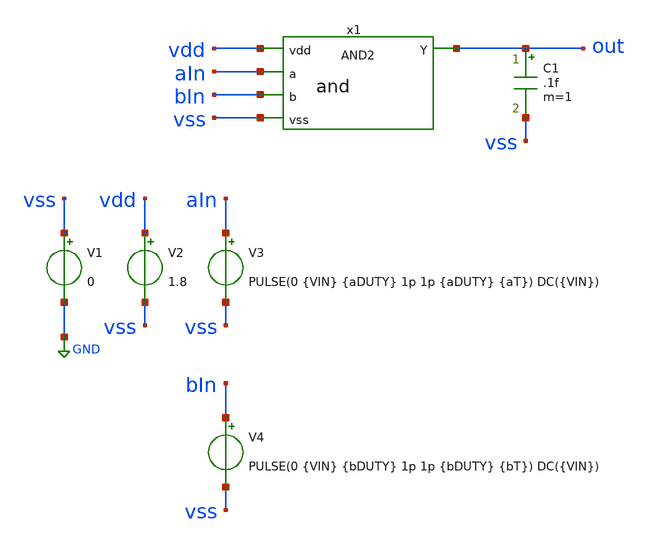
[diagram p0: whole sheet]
** sch_path: eamta2021/sch/and/tbAnd.sch
**.subckt tbAnd
V1 vss GND 0
V2 vdd vss 1.8
V3 aIn vss PULSE(0 {VIN} {aDUTY} 1p 1p {aDUTY} {aT}) DC({VIN})
C1 out vss .1f m=1
V4 bIn vss PULSE(0 {VIN} {bDUTY} 1p 1p {bDUTY} {bT}) DC({VIN})
x1 vdd out aIn bIn vss and
**** begin user architecture code



* parametros
.param VIN=1.8 aT=100n aDUTY=50n bT=200n bDUTY=100n WN=.450 WP=.90
.options TEMP=27.0

* include corners
.lib /home/eamta/skywater/skywater-pdk/libraries/sky130_fd_pr_ngspice/latest/models/corners/sky130.lib TT

* saves
.save all
**PFETs  @M.x1.xm1.msky130_fd_pr__pfet_01v8[id]  @M.x1.xm1.msky130_fd_pr__pfet_01v8[vds]
*+  @M.x1.xm1.msky130_fd_pr__pfet_01v8[vgs]  @M.x1.xm1.msky130_fd_pr__pfet_01v8[vth]  @M.x1.xm2.msky130_fd_pr__pfet_01v8[id]
*+  @M.x1.xm2.msky130_fd_pr__pfet_01v8[vds]  @M.x1.xm2.msky130_fd_pr__pfet_01v8[vgs]  @M.x1.xm2.msky130_fd_pr__pfet_01v8[vth]
*+  @M.x1.xm5.msky130_fd_pr__pfet_01v8[id]  @M.x1.xm5.msky130_fd_pr__pfet_01v8[vds]  @M.x1.xm5.msky130_fd_pr__pfet_01v8[vgs]
*+  @M.x1.xm5.msky130_fd_pr__pfet_01v8[vth]
**NFETs  @M.x1.xm3.msky130_fd_pr__nfet_01v8[id]  @M.x1.xm3.msky130_fd_pr__nfet_01v8[vds]
*+  @M.x1.xm3.msky130_fd_pr__nfet_01v8[vgs]  @M.x1.xm3.msky130_fd_pr__nfet_01v8[vth]  @M.x1.xm4.msky130_fd_pr__nfet_01v8[id]
*+  @M.x1.xm4.msky130_fd_pr__nfet_01v8[vds]  @M.x1.xm4.msky130_fd_pr__nfet_01v8[vgs]  @M.x1.xm4.msky130_fd_pr__nfet_01v8[vth]
*+  @M.x1.xm6.msky130_fd_pr__nfet_01v8[id]  @M.x1.xm6.msky130_fd_pr__nfet_01v8[vds]  @M.x1.xm6.msky130_fd_pr__nfet_01v8[vgs]
*+  @M.x1.xm6.msky130_fd_pr__nfet_01v8[vth]

* SIM
.control
	******************************************************
	*let At=.005ns

	tran 0.005ns 500ns

	setplot tran1
	**comportamiento iiiiiiiiiiiiiiiiiiiiiiiii
	plot v(aIn) v(bIn)+2 v(out)+4
	**rise/fall
	plot v(out) v(aIn) .18 1.62 xlimit 149.95ns 150.15ns
	plot v(out) v(aIn) .18 1.62 xlimit 199.95ns 200.05ns
	**sos inimputable iiiiiiiiiiiiiiiiiii
	*plot tran1.@M.x1.xm1.msky130_fd_pr__nfet_01v8[vds]
	*plot tran1.@M.x1.xm1.msky130_fd_pr__nfet_01v8[id] tran1.@M.x1.xm2.msky130_fd_pr__pfet_01v8[id]

	*set filetype=ascii iiiiiiiiiiiiiiiiiii
	*write simInvTran.raw
	*reset
	******************************************************
	*alterparam bDUTY=100n
	*dc V3 0 1.8 0.01
	*alterparam aDUTY=100n
	*dc V4 0 1.8 0.01
	*dc V3 0 1.8 0.01 V4 0 1.8 0.01

	*setplot dc1iiiiiiiiiiiiii
	*plot dc1.out vs dc1.aIn dc2.out vs dc2.bIn dc3.out vs dc3.aIn
	*plot @M.x1.xm1.msky130_fd_pr__nfet_01v8[id]
	*plot @M.x1.xm1.msky130_fd_pr__nfet_01v8[vd]

	*set filetype=ascii
	*write simInvDc.raw
	*reset
	******************************************************
	op

	set filetype=ascii
	write simInvOp.raw

***********************************************************
	*analisis cuasi parametrico
	*let actParam=1ps
	*let topParam=100ps
	*let detlaParam=10ps

	*foreach x 1ps 10ps 20ps 30ps 40ps 50ps
	*	alterparam THL=$x
	*	tran .01ns .1us
	*	let actParam=actParam+deltaParam
	*	print $x
	*end

	*plot tran1.out tran2.out tran3.out tran4.out tran5.out tran6.out tran7.out tran8.out tran9.out

	print all
.endc

.end


**** end user architecture code
**.ends

* expanding   symbol:  and/and.sym # of pins=5
** sym_path: eamta2021/sch/and/and.sym
** sch_path: eamta2021/sch/and/and.sch
.subckt and vdd Y a b vss
*.ipin vdd
*.ipin vss
*.ipin a
*.ipin b
*.opin Y
XM1 net1 b vdd vdd sky130_fd_pr__pfet_01v8 L=0.15 W={WP} nf=1 ad='int((nf+1)/2) * W/nf * 0.29' as='int((nf+2)/2) * W/nf * 0.29'
+ pd='2*int((nf+1)/2) * (W/nf + 0.29)' ps='2*int((nf+2)/2) * (W/nf + 0.29)' nrd='0.29 / W' nrs='0.29 / W'
+ sa=0 sb=0 sd=0 mult=1 m=1
XM2 net1 a vdd vdd sky130_fd_pr__pfet_01v8 L=0.15 W={WP} nf=1 ad='int((nf+1)/2) * W/nf * 0.29' as='int((nf+2)/2) * W/nf * 0.29'
+ pd='2*int((nf+1)/2) * (W/nf + 0.29)' ps='2*int((nf+2)/2) * (W/nf + 0.29)' nrd='0.29 / W' nrs='0.29 / W'
+ sa=0 sb=0 sd=0 mult=1 m=1
XM3 net1 a net2 vss sky130_fd_pr__nfet_01v8 L=0.15 W={WN} nf=1 ad='int((nf+1)/2) * W/nf * 0.29' as='int((nf+2)/2) * W/nf * 0.29'
+ pd='2*int((nf+1)/2) * (W/nf + 0.29)' ps='2*int((nf+2)/2) * (W/nf + 0.29)' nrd='0.29 / W' nrs='0.29 / W'
+ sa=0 sb=0 sd=0 mult=1 m=1
XM4 net2 b vss vss sky130_fd_pr__nfet_01v8 L=0.15 W={WN} nf=1 ad='int((nf+1)/2) * W/nf * 0.29' as='int((nf+2)/2) * W/nf * 0.29'
+ pd='2*int((nf+1)/2) * (W/nf + 0.29)' ps='2*int((nf+2)/2) * (W/nf + 0.29)' nrd='0.29 / W' nrs='0.29 / W'
+ sa=0 sb=0 sd=0 mult=1 m=1
XM5 Y net1 vdd vdd sky130_fd_pr__pfet_01v8 L=0.15 W={WP} nf=1 ad='int((nf+1)/2) * W/nf * 0.29' as='int((nf+2)/2) * W/nf * 0.29'
+ pd='2*int((nf+1)/2) * (W/nf + 0.29)' ps='2*int((nf+2)/2) * (W/nf + 0.29)' nrd='0.29 / W' nrs='0.29 / W'
+ sa=0 sb=0 sd=0 mult=1 m=1
XM6 Y net1 vss vss sky130_fd_pr__nfet_01v8 L=0.15 W={WN} nf=1 ad='int((nf+1)/2) * W/nf * 0.29' as='int((nf+2)/2) * W/nf * 0.29'
+ pd='2*int((nf+1)/2) * (W/nf + 0.29)' ps='2*int((nf+2)/2) * (W/nf + 0.29)' nrd='0.29 / W' nrs='0.29 / W'
+ sa=0 sb=0 sd=0 mult=1 m=1
.ends

.GLOBAL GND
.end
